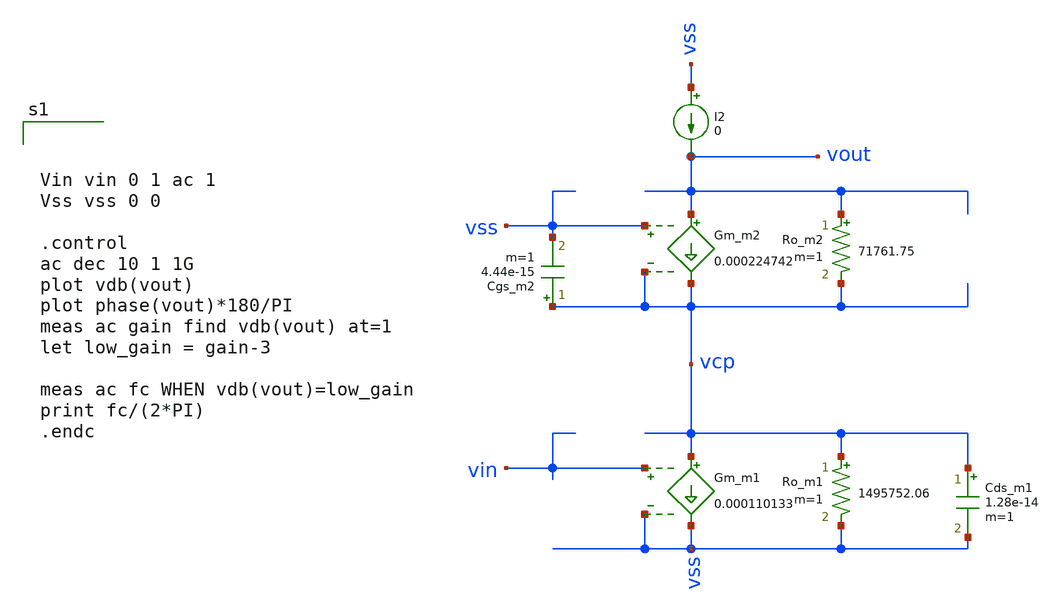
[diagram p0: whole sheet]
** sch_path: test-python/sstadex/untitled-4.sch
**.subckt untitled-4
Ro_m2 vout vcp 71761.75 m=1
Gm_m2 vout vcp vss vcp 0.000224742
Cgs_m2 vcp vss 4.44e-15 m=1
Ro_m1 vcp vss 1495752.06 m=1
Gm_m1 vcp vss vin vss 0.000110133
Cds_m1 vcp vss 1.28e-14 m=1
I2 vss vout 0
**** begin user architecture code



Vin vin 0 1 ac 1
Vss vss 0 0

.control
ac dec 10 1 1G
plot vdb(vout)
plot phase(vout)*180/PI
meas ac gain find vdb(vout) at=1
let low_gain = gain-3

meas ac fc WHEN vdb(vout)=low_gain
print fc/(2*PI)
.endc



**** end user architecture code
**.ends
.end
